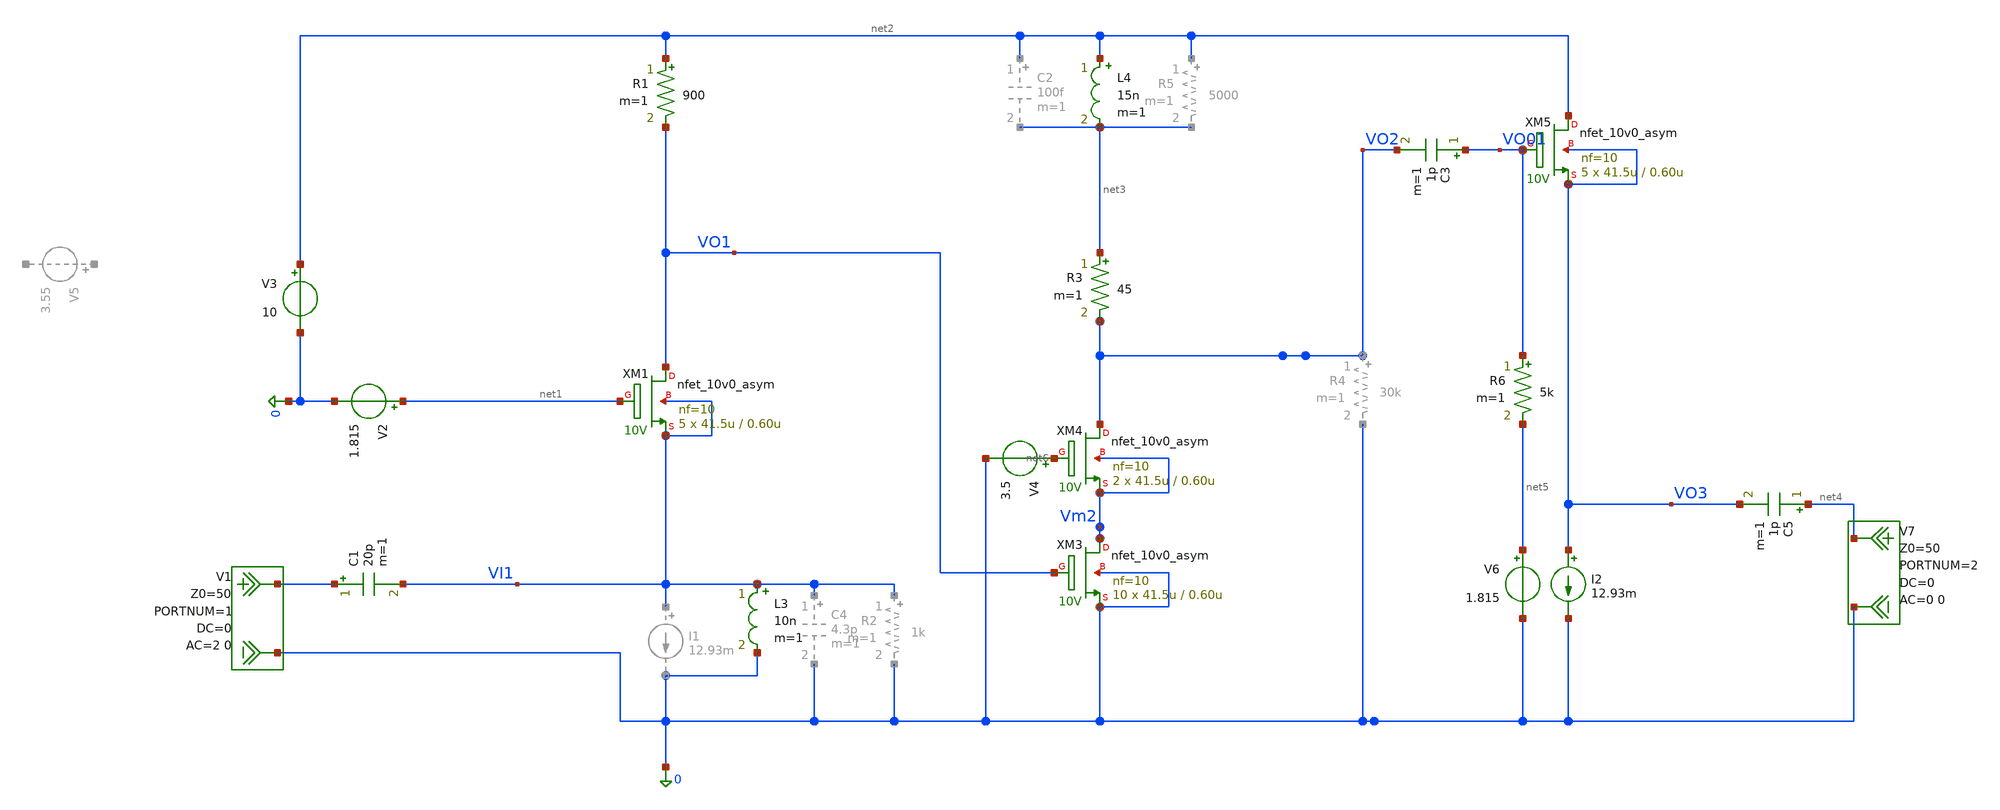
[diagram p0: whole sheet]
** sch_path: 10V0-CG/10V0-CG-STG1.sch
**.subckt 10V0-CG-STG1
XM1 VO1 net1 VI1 VI1 nfet_10v0_asym L=0.60u W=41.5u nf=10 ad='W * 1.48u' as='W * 0.48u' pd='2 * (W + 1.48u)'
+ ps='2 * (W + 0.48u)' nrd=0 nrs=0 sa=0 sb=0 sd=0 m=5
V1 VI1 0 DC 0 AC 2 0 portnum 1 z0 50
V2 net1 0 1.815
V3 net2 0 10
R1 net2 VO1 900 m=1
V7 net4 0 DC 0 AC 0 0 portnum 2 z0 50
L3 VI1 0 10n m=1
XM3 Vm2 VO1 0 0 nfet_10v0_asym L=0.60u W=41.5u nf=10 ad='W * 1.48u' as='W * 0.48u' pd='2 * (W + 1.48u)'
+ ps='2 * (W + 0.48u)' nrd=0 nrs=0 sa=0 sb=0 sd=0 m=10
XM4 VO2 net6 Vm2 Vm2 nfet_10v0_asym L=0.60u W=41.5u nf=10 ad='W * 1.48u' as='W * 0.48u' pd='2 * (W + 1.48u)'
+ ps='2 * (W + 0.48u)' nrd=0 nrs=0 sa=0 sb=0 sd=0 m=2
L4 net2 net3 15n m=1
R3 net3 VO2 45 m=1
V4 net6 0 3.5
XM5 net2 VO01 VO3 VO3 nfet_10v0_asym L=0.60u W=41.5u nf=10 ad='W * 1.48u' as='W * 0.48u' pd='2 * (W + 1.48u)'
+ ps='2 * (W + 0.48u)' nrd=0 nrs=0 sa=0 sb=0 sd=0 m=5
C3 VO01 VO2 1p m=1
I2 VO3 0 12.93m
V6 net5 0 1.815
R6 VO01 net5 5k m=1
C5 net4 VO3 1p m=1
**** begin user architecture code

.include $::180MCU_MODELS/design.ngspice
.lib $::180MCU_MODELS/sm141064.ngspice typical
.lib $::180MCU_MODELS/smbb000149.ngspice typical




.control
op

save all
write 10V0-CG-STG1.raw

set filetype=ascii

echo ================================================== > 10V0-CG-STG1-op-detailed.txt
echo GF180MCU 10V0-CG-STG1 detailed operating point >> 10V0-CG-STG1-op-detailed.txt
echo ================================================== >> 10V0-CG-STG1-op-detailed.txt
echo  >> 10V0-CG-STG1-op-detailed.txt

echo ---- Node voltages and source currents ---- >> 10V0-CG-STG1-op-detailed.txt
print all >> 10V0-CG-STG1-op-detailed.txt
echo  >> 10V0-CG-STG1-op-detailed.txt

echo ---- All device operating point data ---- >> 10V0-CG-STG1-op-detailed.txt
show all >> 10V0-CG-STG1-op-detailed.txt
echo  >> 10V0-CG-STG1-op-detailed.txt

echo ---- Expanded device listing and hierarchy ---- >> 10V0-CG-STG1-op-detailed.txt
listing e >> 10V0-CG-STG1-op-detailed.txt

sp lin 1001 1 10e9 1
write 10V0-CG-STG1-sp.raw

ac lin 1001 1 10e9
write 10V0-CG-STG1-ac.raw

.endc


**** end user architecture code
**.ends
.end
